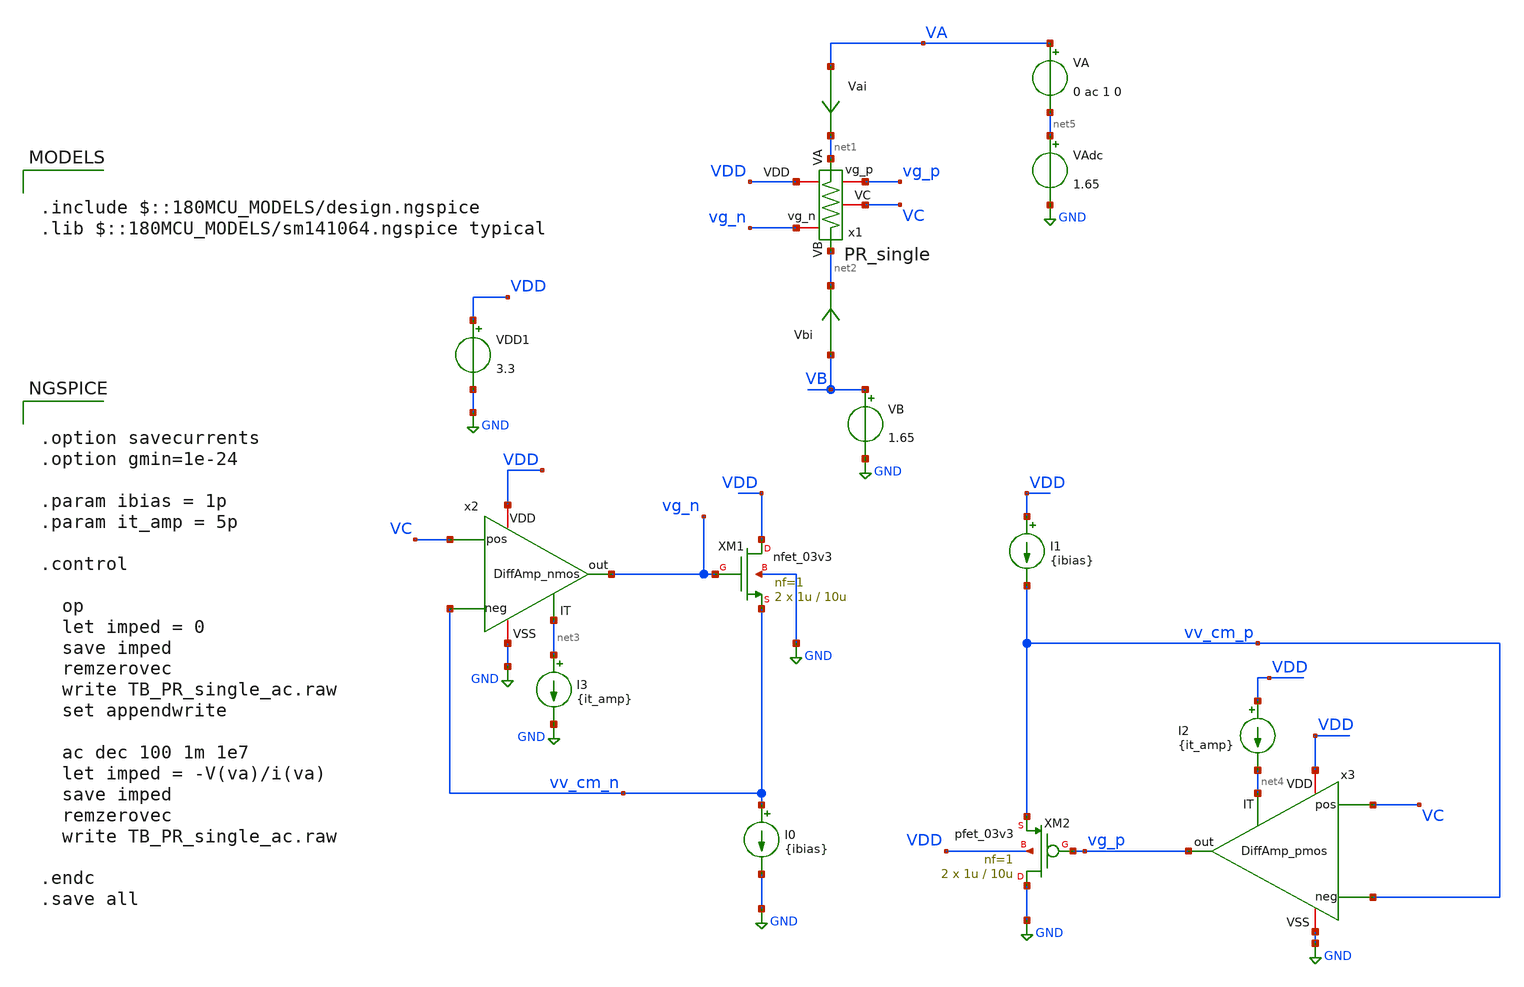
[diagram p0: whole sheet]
** sch_path: TIA/xschem/pseudo_res_dir/TB_PR_single_ac.sch
**.subckt TB_PR_single_ac
x1 VDD net1 vg_p VC vg_n net2 PR_single
XM1 VDD vg_n vv_cm_n GND nfet_03v3 L=10u W=1u nf=1 ad='int((nf+1)/2) * W/nf * 0.18u' as='int((nf+2)/2) * W/nf * 0.18u'
+ pd='2*int((nf+1)/2) * (W/nf + 0.18u)' ps='2*int((nf+2)/2) * (W/nf + 0.18u)' nrd='0.18u / W' nrs='0.18u / W'
+ sa=0 sb=0 sd=0 m=2
XM2 GND vg_p vv_cm_p VDD pfet_03v3 L=10u W=1u nf=1 ad='int((nf+1)/2) * W/nf * 0.18u' as='int((nf+2)/2) * W/nf * 0.18u'
+ pd='2*int((nf+1)/2) * (W/nf + 0.18u)' ps='2*int((nf+2)/2) * (W/nf + 0.18u)' nrd='0.18u / W' nrs='0.18u / W'
+ sa=0 sb=0 sd=0 m=2
I0 vv_cm_n GND {ibias}
I1 VDD vv_cm_p {ibias}
VDD1 VDD GND 3.3
Vai VA net1 0
.save i(vai)
Vbi VB net2 0
.save i(vbi)
x2 VDD GND VC vv_cm_n net3 vg_n DiffAmp_nmos
I2 VDD net4 {it_amp}
x3 VDD GND net4 vv_cm_p VC vg_p DiffAmp_pmos
I3 net3 GND {it_amp}
VA VA net5 0 ac 1 0
VB VB GND 1.65
VAdc net5 GND 1.65
**** begin user architecture code

.include $::180MCU_MODELS/design.ngspice
.lib $::180MCU_MODELS/sm141064.ngspice typical



.option savecurrents
.option gmin=1e-24

.param ibias = 1p
.param it_amp = 5p

.control

  op
  let imped = 0
  save imped
  remzerovec
  write TB_PR_single_ac.raw
  set appendwrite

  ac dec 100 1m 1e7
  let imped = -V(va)/i(va)
  save imped
  remzerovec
  write TB_PR_single_ac.raw

.endc
.save all


**** end user architecture code
**.ends
.GLOBAL GND
.end
